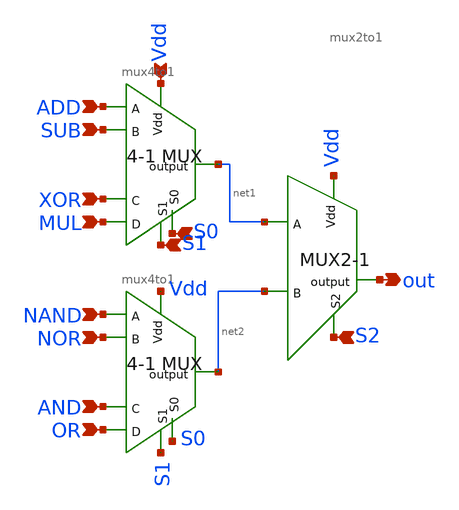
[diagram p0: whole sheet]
** sch_path: extra_stuff/mux8to1.sch
**.subckt mux8to1 Vdd S0 S1 S2 out ADD SUB XOR MUL NAND NOR AND OR
*.ipin Vdd
*.ipin S0
*.ipin S1
*.ipin S2
*.opin out
*.ipin ADD
*.ipin SUB
*.ipin XOR
*.ipin MUL
*.ipin NAND
*.ipin NOR
*.ipin AND
*.ipin OR
x2 net1 ADD SUB XOR MUL Vdd S0 S1 mux4to1
x3 out Vdd net1 net2 S2 mux2to1
x1 net2 NAND NOR AND OR Vdd S0 S1 mux4to1
**.ends
.end
